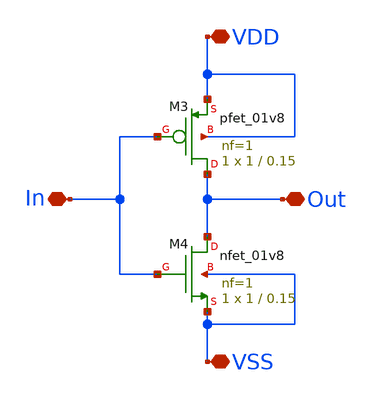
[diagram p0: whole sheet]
** sch_path: HVT/xschem_pruebas/inv_prueba.sch
**.subckt inv_prueba Out In VDD VSS
*.iopin Out
*.iopin In
*.iopin VDD
*.iopin VSS
XM3 Out In VDD VDD sky130_fd_pr__pfet_01v8 L=0.15 W=1 nf=1 ad='int((nf+1)/2) * W/nf * 0.29' as='int((nf+2)/2) * W/nf * 0.29'
+ pd='2*int((nf+1)/2) * (W/nf + 0.29)' ps='2*int((nf+2)/2) * (W/nf + 0.29)' nrd='0.29 / W' nrs='0.29 / W'
+ sa=0 sb=0 sd=0 mult=1 m=1
XM4 Out In VSS VSS sky130_fd_pr__nfet_01v8 L=0.15 W=1 nf=1 ad='int((nf+1)/2) * W/nf * 0.29' as='int((nf+2)/2) * W/nf * 0.29'
+ pd='2*int((nf+1)/2) * (W/nf + 0.29)' ps='2*int((nf+2)/2) * (W/nf + 0.29)' nrd='0.29 / W' nrs='0.29 / W'
+ sa=0 sb=0 sd=0 mult=1 m=1
**.ends
.end
